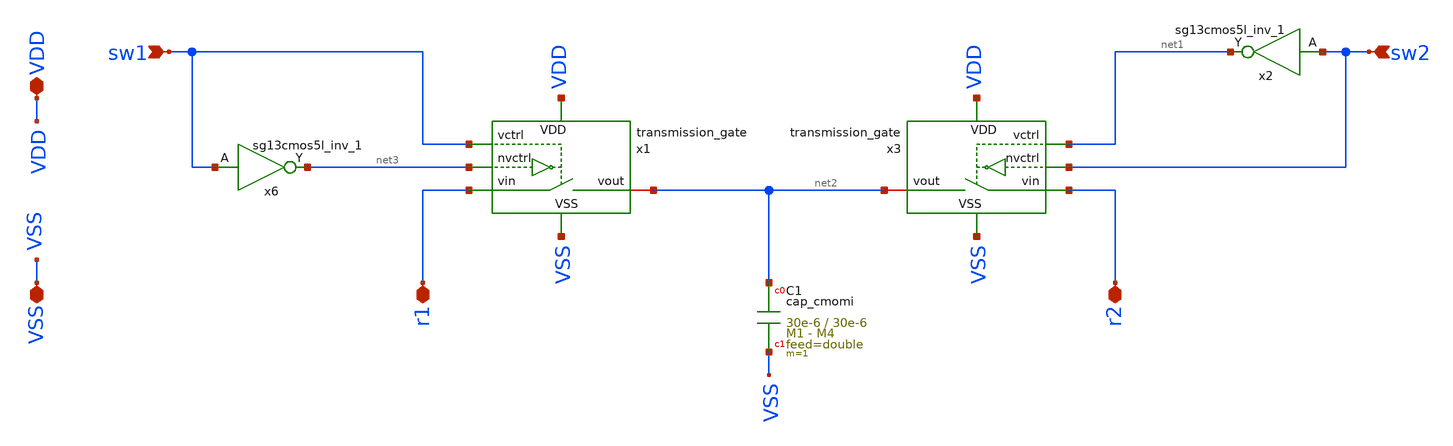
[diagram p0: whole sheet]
** sch_path: macros/heichips26_vcr/macros/switched_capacitor/schematic/xschem/switched_cap_cell.sch
**.subckt switched_cap_cell sw1 r1 r2 VDD VSS sw2
*.ipin sw1
*.iopin r1
*.iopin r2
*.iopin VDD
*.iopin VSS
*.ipin sw2
x1 sw1 r1 net2 net3 VDD VSS transmission_gate
x3 net1 r2 net2 sw2 VDD VSS transmission_gate
x6 net3 sw1 VDD VSS sg13cmos5l_inv_1
x2 net1 sw2 VDD VSS sg13cmos5l_inv_1
XC1 net2 VSS cap_cmomi w=30e-6 l=30e-6 mmin=1 mmax=4 feed=double subblock=0 m=1 mm_ok=1
**.ends

* expanding   symbol:  transmission_gate.sym # of pins=6
** sym_path: macros/heichips26_vcr/macros/switched_capacitor/schematic/xschem/transmission_gate.sym
** sch_path: macros/heichips26_vcr/macros/switched_capacitor/schematic/xschem/transmission_gate.sch
.subckt transmission_gate vctrl vin vout nvctrl VDD VSS
*.iopin vin
*.iopin vout
*.ipin vctrl
*.ipin nvctrl
*.iopin VDD
*.iopin VSS
XM3 vout vctrl vin VSS sg13_hv_nmos w={tg_ngate_w*tg_ng} l={tg_ch_len} ng={tg_ng} m=1 mm_ok=1
XM4 vout nvctrl vin VDD sg13_hv_pmos w={tg_pgate_w*tg_ng} l={tg_ch_len} ng={tg_ng} m=1 mm_ok=1
**** begin user architecture code


.param tg_ch_len=1u
.param tg_ngate_w=2u
.param tg_pgate_w=10u
.param tg_ng=20


**** end user architecture code
.ends

.end
